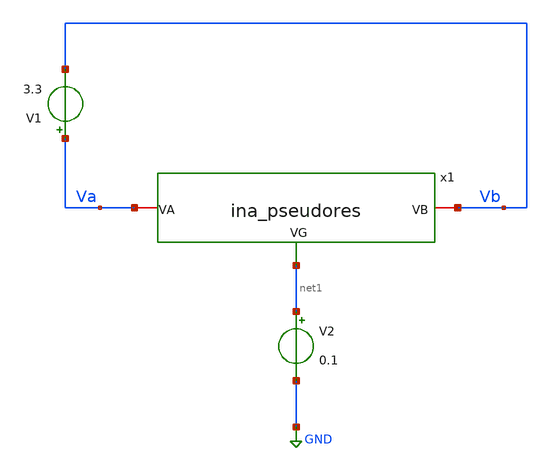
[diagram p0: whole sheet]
** sch_path: designs/libs/tb_ina/tb_ina_pseudores_dc/tb_ina_pseudores_dc.sch
**.subckt tb_ina_pseudores_dc
V1 Va Vb 3.3
V2 net1 GND 0.1
x1 Va Vb net1 ina_pseudores
**** begin user architecture code

.include $::180MCU_MODELS/design.ngspice
.lib $::180MCU_MODELS/sm141064.ngspice typical
.lib $::180MCU_MODELS/sm141064.ngspice cap_mim
.lib $::180MCU_MODELS/sm141064.ngspice moscap_typical
.lib $::180MCU_MODELS/sm141064.ngspice mimcap_typical
.lib $::180MCU_MODELS/sm141064.ngspice res_typical
* .lib $::180MCU_MODELS/sm141064.ngspice res_statistical
* ngspice commands




.control
save all

set color0 = white

*************************************
** PARAMETERS
*************************************

let Vg = 0.1

*************************************
** SOURCES
*************************************

alter @V1[DC] = 0
alter @V2[DC] = $&Vg


*************************************
** DC SWEEP SIMULATION
*************************************

dc V1 -1.65 1.65 0.001

*************************************
** PLOTS
*************************************

setplot dc1
let Va = v(Va)
let Vb = v(Vb)
let Vin = Va-Vb
let Iin = -1*i(v1)
let Req = Vin/Iin
plot Req
print Req

*************************************
** SAVE
*************************************

write tb_ina_pseudores_dc.raw

.endc
* ngspice commands



**** end user architecture code
**.ends

* expanding   symbol:  libs/core_ina/ina_pseudores/ina_pseudores.sym # of pins=3
** sym_path: designs/libs/core_ina/ina_pseudores/ina_pseudores.sym
** sch_path: designs/libs/core_ina/ina_pseudores/ina_pseudores.sch
.subckt ina_pseudores VA VB VG
*.ipin Vg
*.iopin Va
*.iopin Vb
XM1 Va Vg Vg Vg nfet_03v3 L=5u W=0.28u nf=1 ad='int((nf+1)/2) * W/nf * 0.18u' as='int((nf+2)/2) * W/nf * 0.18u'
+ pd='2*int((nf+1)/2) * (W/nf + 0.18u)' ps='2*int((nf+2)/2) * (W/nf + 0.18u)' nrd='0.18u / W' nrs='0.18u / W'
+ sa=0 sb=0 sd=0 m=1
XM2 net2 Vg Vg Vg nfet_03v3 L=5u W=0.28u nf=1 ad='int((nf+1)/2) * W/nf * 0.18u' as='int((nf+2)/2) * W/nf * 0.18u'
+ pd='2*int((nf+1)/2) * (W/nf + 0.18u)' ps='2*int((nf+2)/2) * (W/nf + 0.18u)' nrd='0.18u / W' nrs='0.18u / W'
+ sa=0 sb=0 sd=0 m=1
XM3 net2 net1 net1 net1 nfet_03v3 L=15u W=0.28u nf=1 ad='int((nf+1)/2) * W/nf * 0.18u' as='int((nf+2)/2) * W/nf * 0.18u'
+ pd='2*int((nf+1)/2) * (W/nf + 0.18u)' ps='2*int((nf+2)/2) * (W/nf + 0.18u)' nrd='0.18u / W' nrs='0.18u / W'
+ sa=0 sb=0 sd=0 m=1
XM4 Vb net1 net1 net1 nfet_03v3 L=15u W=0.28u nf=1 ad='int((nf+1)/2) * W/nf * 0.18u' as='int((nf+2)/2) * W/nf * 0.18u'
+ pd='2*int((nf+1)/2) * (W/nf + 0.18u)' ps='2*int((nf+2)/2) * (W/nf + 0.18u)' nrd='0.18u / W' nrs='0.18u / W'
+ sa=0 sb=0 sd=0 m=1
.ends

.GLOBAL GND
.end
